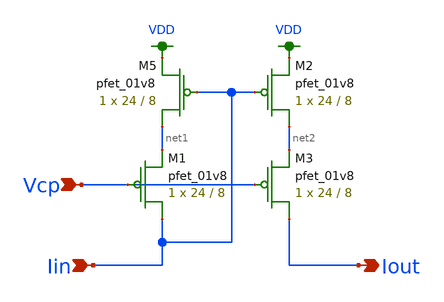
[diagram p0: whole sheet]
** sch_path: modules/cascode_current_mirror.sch
**.subckt cascode_current_mirror Vcp Iin Iout
*.ipin Vcp
*.ipin Iin
*.opin Iout
XM5 net1 Iin VDD VDD sky130_fd_pr__pfet_01v8 L=8 W=24 nf=1 ad='int((nf+1)/2) * W/nf * 0.29' as='int((nf+2)/2) * W/nf * 0.29'
+ pd='2*int((nf+1)/2) * (W/nf + 0.29)' ps='2*int((nf+2)/2) * (W/nf + 0.29)' nrd='0.29 / W' nrs='0.29 / W'
+ sa=0 sb=0 sd=0 mult=1 m=1
XM1 Iin Vcp net1 VDD sky130_fd_pr__pfet_01v8 L=8 W=24 nf=1 ad='int((nf+1)/2) * W/nf * 0.29' as='int((nf+2)/2) * W/nf * 0.29'
+ pd='2*int((nf+1)/2) * (W/nf + 0.29)' ps='2*int((nf+2)/2) * (W/nf + 0.29)' nrd='0.29 / W' nrs='0.29 / W'
+ sa=0 sb=0 sd=0 mult=1 m=1
XM2 net2 Iin VDD VDD sky130_fd_pr__pfet_01v8 L=8 W=24 nf=1 ad='int((nf+1)/2) * W/nf * 0.29' as='int((nf+2)/2) * W/nf * 0.29'
+ pd='2*int((nf+1)/2) * (W/nf + 0.29)' ps='2*int((nf+2)/2) * (W/nf + 0.29)' nrd='0.29 / W' nrs='0.29 / W'
+ sa=0 sb=0 sd=0 mult=1 m=1
XM3 Iout Vcp net2 VDD sky130_fd_pr__pfet_01v8 L=8 W=24 nf=1 ad='int((nf+1)/2) * W/nf * 0.29' as='int((nf+2)/2) * W/nf * 0.29'
+ pd='2*int((nf+1)/2) * (W/nf + 0.29)' ps='2*int((nf+2)/2) * (W/nf + 0.29)' nrd='0.29 / W' nrs='0.29 / W'
+ sa=0 sb=0 sd=0 mult=1 m=1
**.ends
.GLOBAL VDD
.end
